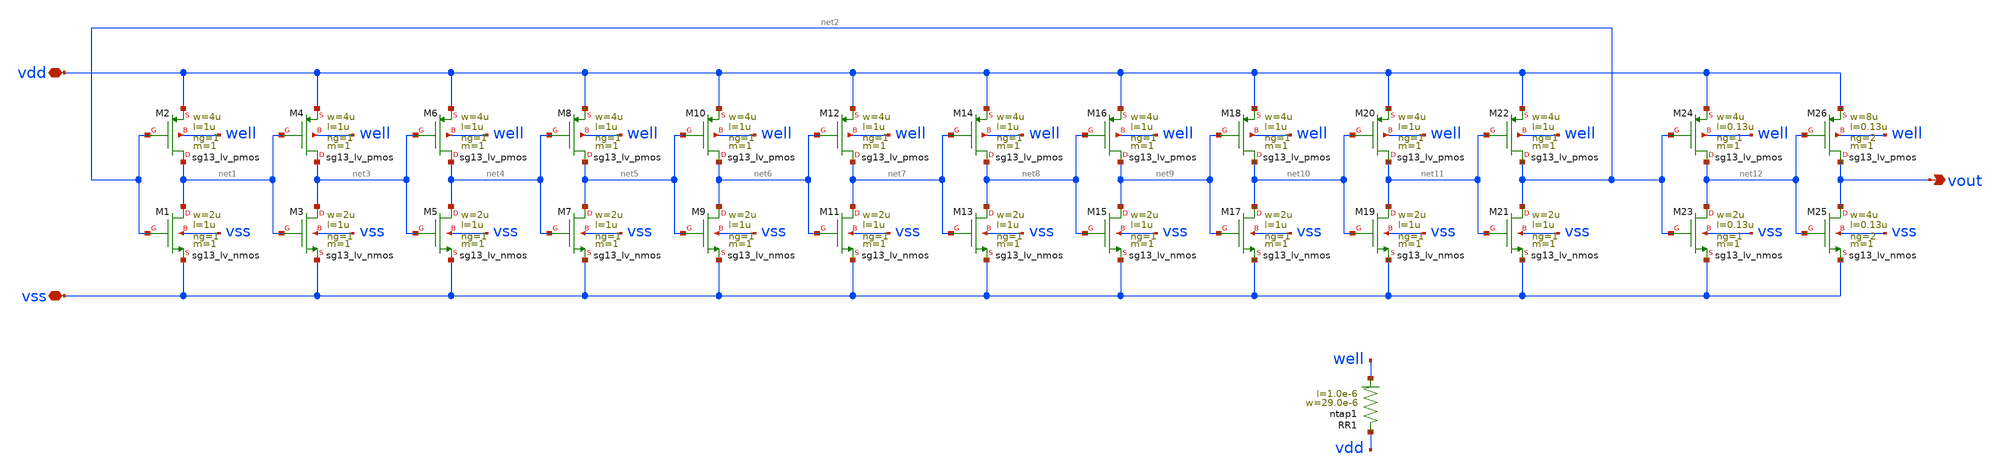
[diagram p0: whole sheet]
** sch_path: Layouts/cgenerator/cgenerator.sch
**.subckt cgenerator vdd vss vout
*.iopin vdd
*.iopin vss
*.opin vout
XM1 net1 net2 vss vss sg13_lv_nmos w=2u l=1u ng=1 m=1 mm_ok=1
XM2 net1 net2 vdd well sg13_lv_pmos w=4u l=1u ng=1 m=1 mm_ok=1
XM3 net3 net1 vss vss sg13_lv_nmos w=2u l=1u ng=1 m=1 mm_ok=1
XM4 net3 net1 vdd well sg13_lv_pmos w=4u l=1u ng=1 m=1 mm_ok=1
XM5 net4 net3 vss vss sg13_lv_nmos w=2u l=1u ng=1 m=1 mm_ok=1
XM6 net4 net3 vdd well sg13_lv_pmos w=4u l=1u ng=1 m=1 mm_ok=1
XM7 net5 net4 vss vss sg13_lv_nmos w=2u l=1u ng=1 m=1 mm_ok=1
XM8 net5 net4 vdd well sg13_lv_pmos w=4u l=1u ng=1 m=1 mm_ok=1
XM9 net6 net5 vss vss sg13_lv_nmos w=2u l=1u ng=1 m=1 mm_ok=1
XM10 net6 net5 vdd well sg13_lv_pmos w=4u l=1u ng=1 m=1 mm_ok=1
XM11 net7 net6 vss vss sg13_lv_nmos w=2u l=1u ng=1 m=1 mm_ok=1
XM12 net7 net6 vdd well sg13_lv_pmos w=4u l=1u ng=1 m=1 mm_ok=1
XM13 net8 net7 vss vss sg13_lv_nmos w=2u l=1u ng=1 m=1 mm_ok=1
XM14 net8 net7 vdd well sg13_lv_pmos w=4u l=1u ng=1 m=1 mm_ok=1
XM15 net9 net8 vss vss sg13_lv_nmos w=2u l=1u ng=1 m=1 mm_ok=1
XM16 net9 net8 vdd well sg13_lv_pmos w=4u l=1u ng=1 m=1 mm_ok=1
XM17 net10 net9 vss vss sg13_lv_nmos w=2u l=1u ng=1 m=1 mm_ok=1
XM18 net10 net9 vdd well sg13_lv_pmos w=4u l=1u ng=1 m=1 mm_ok=1
XM19 net11 net10 vss vss sg13_lv_nmos w=2u l=1u ng=1 m=1 mm_ok=1
XM20 net11 net10 vdd well sg13_lv_pmos w=4u l=1u ng=1 m=1 mm_ok=1
XM21 net2 net11 vss vss sg13_lv_nmos w=2u l=1u ng=1 m=1 mm_ok=1
XM22 net2 net11 vdd well sg13_lv_pmos w=4u l=1u ng=1 m=1 mm_ok=1
XM23 net12 net2 vss vss sg13_lv_nmos w=2u l=0.13u ng=1 m=1 mm_ok=1
XM24 net12 net2 vdd well sg13_lv_pmos w=4u l=0.13u ng=1 m=1 mm_ok=1
XM26 vout net12 vdd well sg13_lv_pmos w=8u l=0.13u ng=2 m=1 mm_ok=1
XM25 vout net12 vss vss sg13_lv_nmos w=4u l=0.13u ng=2 m=1 mm_ok=1
XR1 vdd well ntap1 R=11.01 w=29.0e-6 l=1.0e-6
**.ends
.end
